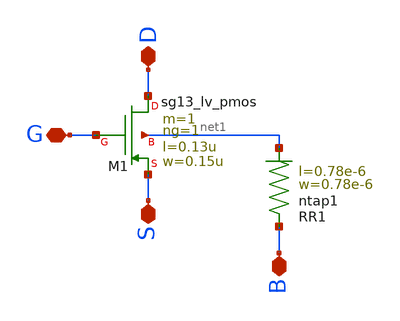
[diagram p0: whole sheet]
** sch_path: ihp-sg13g2/schematic/xschem/sg13_lv_pmos_tap.sch
**.subckt sg13_lv_pmos_tap D S G B
*.iopin D
*.iopin S
*.iopin G
*.iopin B
XM1 D G S net1 sg13_lv_pmos w=0.15u l=0.13u ng=1 m=1 mm_ok=1
XR1 B net1 ntap1 R=262.8 w=0.78e-6 l=0.78e-6
**.ends
.end
